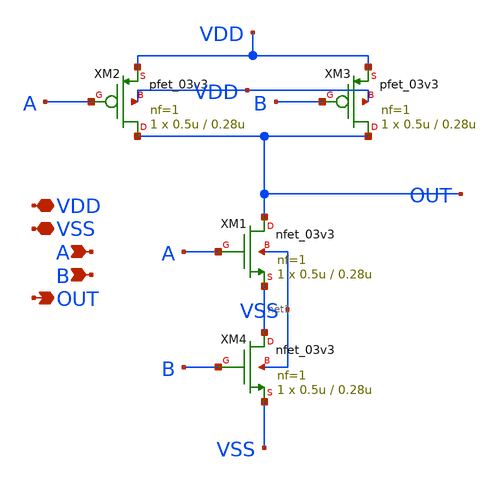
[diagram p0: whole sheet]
** sch_path: DAC_PAKISTAN_01/Pakistan1_Xschem/NAND.sch
**.subckt NAND VDD VSS A B OUT
*.iopin VDD
*.iopin VSS
*.ipin A
*.ipin B
*.opin OUT
XM2 OUT A VDD VDD pfet_03v3 L=0.28u W=0.5u nf=1 ad='int((nf+1)/2) * W/nf * 0.18u' as='int((nf+2)/2) * W/nf * 0.18u'
+ pd='2*int((nf+1)/2) * (W/nf + 0.18u)' ps='2*int((nf+2)/2) * (W/nf + 0.18u)' nrd='0.18u / W' nrs='0.18u / W'
+ sa=0 sb=0 sd=0 m=1
XM3 OUT B VDD VDD pfet_03v3 L=0.28u W=0.5u nf=1 ad='int((nf+1)/2) * W/nf * 0.18u' as='int((nf+2)/2) * W/nf * 0.18u'
+ pd='2*int((nf+1)/2) * (W/nf + 0.18u)' ps='2*int((nf+2)/2) * (W/nf + 0.18u)' nrd='0.18u / W' nrs='0.18u / W'
+ sa=0 sb=0 sd=0 m=1
XM1 OUT A net1 VSS nfet_03v3 L=0.28u W=0.5u nf=1 ad='int((nf+1)/2) * W/nf * 0.18u' as='int((nf+2)/2) * W/nf * 0.18u'
+ pd='2*int((nf+1)/2) * (W/nf + 0.18u)' ps='2*int((nf+2)/2) * (W/nf + 0.18u)' nrd='0.18u / W' nrs='0.18u / W'
+ sa=0 sb=0 sd=0 m=1
XM4 net1 B VSS VSS nfet_03v3 L=0.28u W=0.5u nf=1 ad='int((nf+1)/2) * W/nf * 0.18u' as='int((nf+2)/2) * W/nf * 0.18u'
+ pd='2*int((nf+1)/2) * (W/nf + 0.18u)' ps='2*int((nf+2)/2) * (W/nf + 0.18u)' nrd='0.18u / W' nrs='0.18u / W'
+ sa=0 sb=0 sd=0 m=1
**.ends
.end
